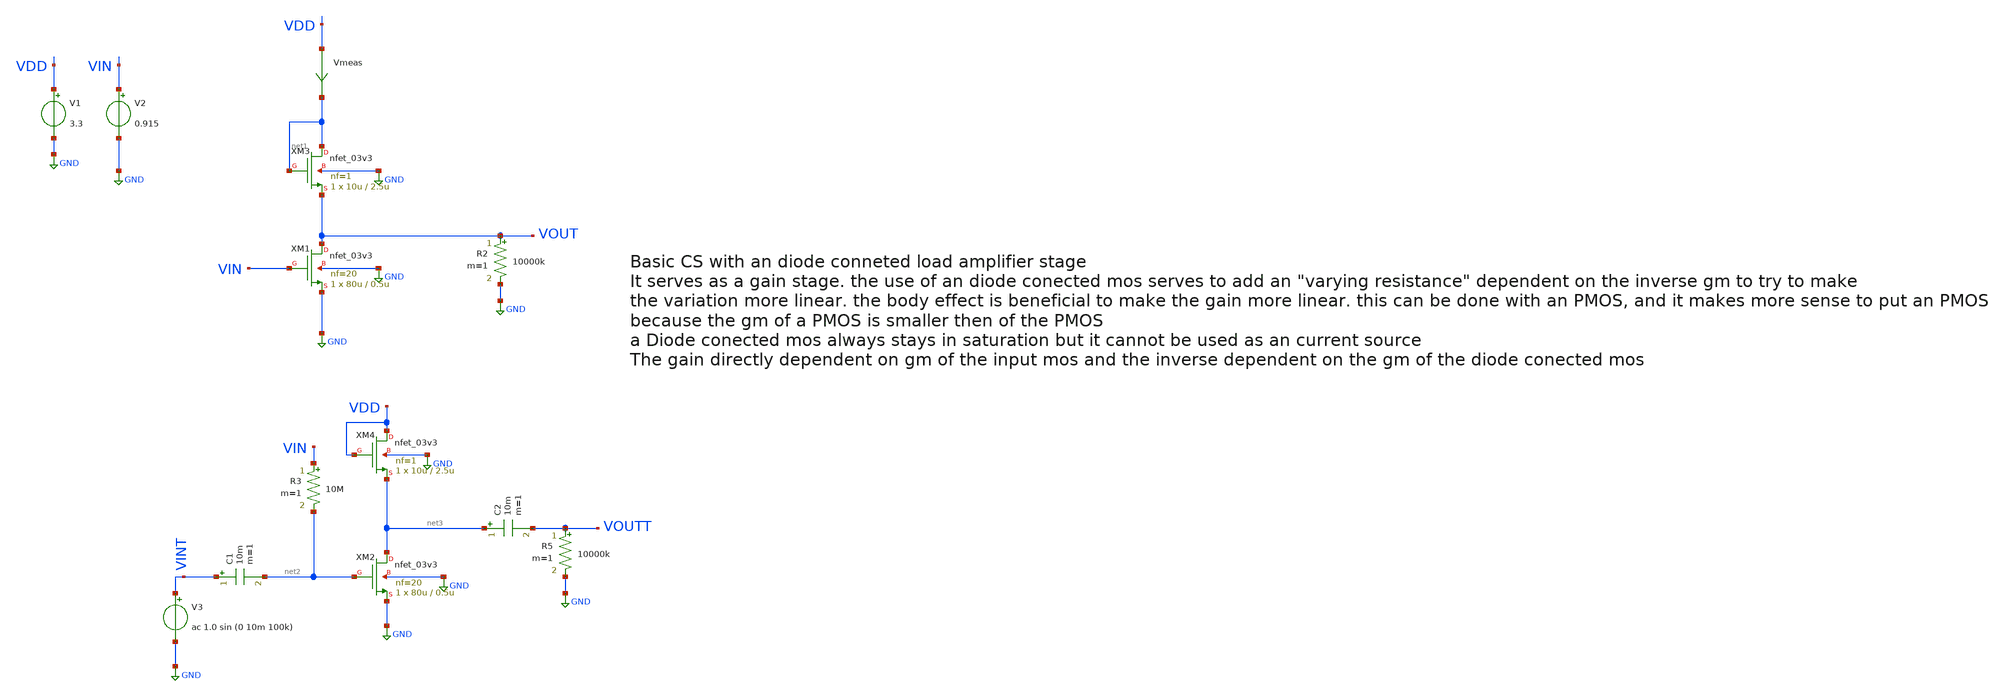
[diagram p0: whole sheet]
** sch_path: basic_circuits/cs_diode_conected_stage.sch
**.subckt cs_diode_conected_stage
XM1 VOUT VIN GND GND nfet_03v3 L=0.5u W=80u nf=20 ad='int((nf+1)/2) * W/nf * 0.18u' as='int((nf+2)/2) * W/nf * 0.18u'
+ pd='2*int((nf+1)/2) * (W/nf + 0.18u)' ps='2*int((nf+2)/2) * (W/nf + 0.18u)' nrd='0.18u / W' nrs='0.18u / W'
+ sa=0 sb=0 sd=0 m=1
Vmeas VDD net1 0
.save i(vmeas)
V1 VDD GND 3.3
V2 VIN GND 0.915
V3 VINT GND ac 1.0 sin (0 10m 100k)
R2 VOUT GND 10000k m=1
C1 VINT net2 10m m=1
R3 VIN net2 10M m=1
C2 net3 VOUTT 10m m=1
R5 VOUTT GND 10000k m=1
XM2 net3 net2 GND GND nfet_03v3 L=0.5u W=80u nf=20 ad='int((nf+1)/2) * W/nf * 0.18u' as='int((nf+2)/2) * W/nf * 0.18u'
+ pd='2*int((nf+1)/2) * (W/nf + 0.18u)' ps='2*int((nf+2)/2) * (W/nf + 0.18u)' nrd='0.18u / W' nrs='0.18u / W'
+ sa=0 sb=0 sd=0 m=1
XM3 net1 net1 VOUT GND nfet_03v3 L=2.5u W=10u nf=1 ad='int((nf+1)/2) * W/nf * 0.18u' as='int((nf+2)/2) * W/nf * 0.18u'
+ pd='2*int((nf+1)/2) * (W/nf + 0.18u)' ps='2*int((nf+2)/2) * (W/nf + 0.18u)' nrd='0.18u / W' nrs='0.18u / W'
+ sa=0 sb=0 sd=0 m=1
XM4 VDD VDD net3 GND nfet_03v3 L=2.5u W=10u nf=1 ad='int((nf+1)/2) * W/nf * 0.18u' as='int((nf+2)/2) * W/nf * 0.18u'
+ pd='2*int((nf+1)/2) * (W/nf + 0.18u)' ps='2*int((nf+2)/2) * (W/nf + 0.18u)' nrd='0.18u / W' nrs='0.18u / W'
+ sa=0 sb=0 sd=0 m=1
**** begin user architecture code

**************************************************************
**************************************************************
**************************************************************
**************************************************************
**************************************************************
*LIBs*********************************************************
**************************************************************
**************************************************************
**************************************************************
**************************************************************
**************************************************************
.include $::180MCU_MODELS/design.ngspice
*.lib $::180MCU_MODELS/sm141064.ngspice statistical *use statistical if you want global and parameter mismatch
*.lib $::180MCU_MODELS/sm141064.ngspice res_statistical
.lib $::180MCU_MODELS/sm141064.ngspice typical
.lib $::180MCU_MODELS/sm141064.ngspice res_typical
.lib $::180MCU_MODELS/sm141064.ngspice moscap_typical
.lib $::180MCU_MODELS/sm141064.ngspice bjt_typical
.lib $::180MCU_MODELS/sm141064.ngspice diode_typical
.lib $::180MCU_MODELS/sm141064.ngspice mimcap_typical
**************************************************************
**************************************************************
**************************************************************
**************************************************************
**************************************************************
*Corners/montecarlo options***********************************
**************************************************************
**************************************************************
**************************************************************
**************************************************************
**************************************************************
.TEMP 27
.param   sw_stat_global = 1   sw_stat_mism = 1  mc_skew = 3  res_mc_skew = 3  cap_mc_skew = 3
+  fnoicor = 1
**************************************************************
**************************************************************
**************************************************************
**************************************************************
*SIMULATION and Plots*****************************************
**************************************************************
**************************************************************
**************************************************************
**************************************************************
.control
save all
dc V2 0 3.3 0.01
*dc simulation
plot v(VOUT) v(VIN) deriv(v(VOUT))
*ploting VIN VOUT and the voltage gain
plot i(Vmeas)
*ploting the current for curiosity
tran 1ns 20u
*transient simulation
plot (v(VINT)) (v(VOUTT))
*simple plot to exemplify the gain
fft v(VOUTT) v(VINT)
*fast fourier transfor
plot mag(v(VOUTT)) mag(v(VINT))
* analyse the frequency spectrum of the transient waves, to detect distortion
ac dec 20 1 50G
*simple ac simulation
plot v(VOUTT)
*gain in function of the input frequency
.endc

**** end user architecture code
**.ends
.GLOBAL GND
.end
